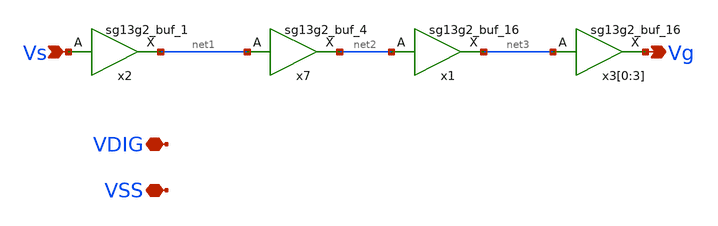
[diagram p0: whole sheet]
** sch_path: AC3E_USM_TDBUCK/design_data/xschem/BUFFLV/BUFFLV_vto1p1.sch
* IHP-GmbH/IHP-Open-PDK/ihp-sg13g2/libs.tech/xschem/sg13g2_stdcells/sg13g2_buf_1.sch:
* Copyright 2023 IHP PDK Authors
* Licensed under the Apache License, Version 2.0 (the "License");
**.subckt BUFFLV_vto1p1 VDIG Vs Vg VSS
*.iopin VDIG
*.ipin Vs
*.opin Vg
*.iopin VSS
x7 net2 net1 VDIG VSS sg13g2_buf_4
x2 net1 Vs VDIG VSS sg13g2_buf_1
x1 net3 net2 VDIG VSS sg13g2_buf_16
x3[0] Vg net3 VDIG VSS sg13g2_buf_16
x3[1] Vg net3 VDIG VSS sg13g2_buf_16
x3[2] Vg net3 VDIG VSS sg13g2_buf_16
x3[3] Vg net3 VDIG VSS sg13g2_buf_16
**.ends

* expanding   symbol:  sg13g2_stdcells/sg13g2_buf_4.sym # of pins=2
** sym_path: sg13g2_stdcells/sg13g2_buf_4.sym
** sch_path: sg13g2_stdcells/sg13g2_buf_4.sch
.subckt sg13g2_buf_4 X A VDD VSS
*.ipin A
*.opin X
*.iopin VDD
*.iopin VSS
XM1 net1 A VSS VSS sg13_lv_nmos w=740.00n l=130.00n ng=1 m=1 mm_ok=1
XM2 X net1 VSS VSS sg13_lv_nmos w=2.96u l=130.00n ng=4 m=1 mm_ok=1
XM3 net1 A VDD VDD sg13_lv_pmos w=1.68u l=130.00n ng=2 m=1 mm_ok=1
XM4 X net1 VDD VDD sg13_lv_pmos w=4.48u l=130.00n ng=4 m=1 mm_ok=1
.ends


* expanding   symbol:  sg13g2_stdcells/sg13g2_buf_1.sym # of pins=2
** sym_path: sg13g2_stdcells/sg13g2_buf_1.sym
** sch_path: sg13g2_stdcells/sg13g2_buf_1.sch
.subckt sg13g2_buf_1 X A VDD VSS
*.ipin A
*.opin X
*.iopin VDD
*.iopin VSS
XM1 net1 A VSS VSS sg13_lv_nmos w=550.00n l=130.00n ng=1 m=1 mm_ok=1
XM2 X net1 VSS VSS sg13_lv_nmos w=740.00n l=130.00n ng=1 m=1 mm_ok=1
XM3 net1 A VDD VDD sg13_lv_pmos w=840.00n l=130.00n ng=1 m=1 mm_ok=1
XM4 X net1 VDD VDD sg13_lv_pmos w=1.12u l=130.00n ng=1 m=1 mm_ok=1
.ends


* expanding   symbol:  sg13g2_stdcells/sg13g2_buf_16.sym # of pins=2
** sym_path: sg13g2_stdcells/sg13g2_buf_16.sym
** sch_path: sg13g2_stdcells/sg13g2_buf_16.sch
.subckt sg13g2_buf_16 X A VDD VSS
*.ipin A
*.opin X
*.iopin VDD
*.iopin VSS
XM1 net1 A VSS VSS sg13_lv_nmos w=4.44u l=130.00n ng=6 m=1 mm_ok=1
XM2 X net1 VSS VSS sg13_lv_nmos w=11.84u l=130.00n ng=16 m=1 mm_ok=1
XM3 net1 A VDD VDD sg13_lv_pmos w=6.72u l=130.00n ng=6 m=1 mm_ok=1
XM4 X net1 VDD VDD sg13_lv_pmos w=17.92u l=130.00n ng=16 m=1 mm_ok=1
.ends

.end
